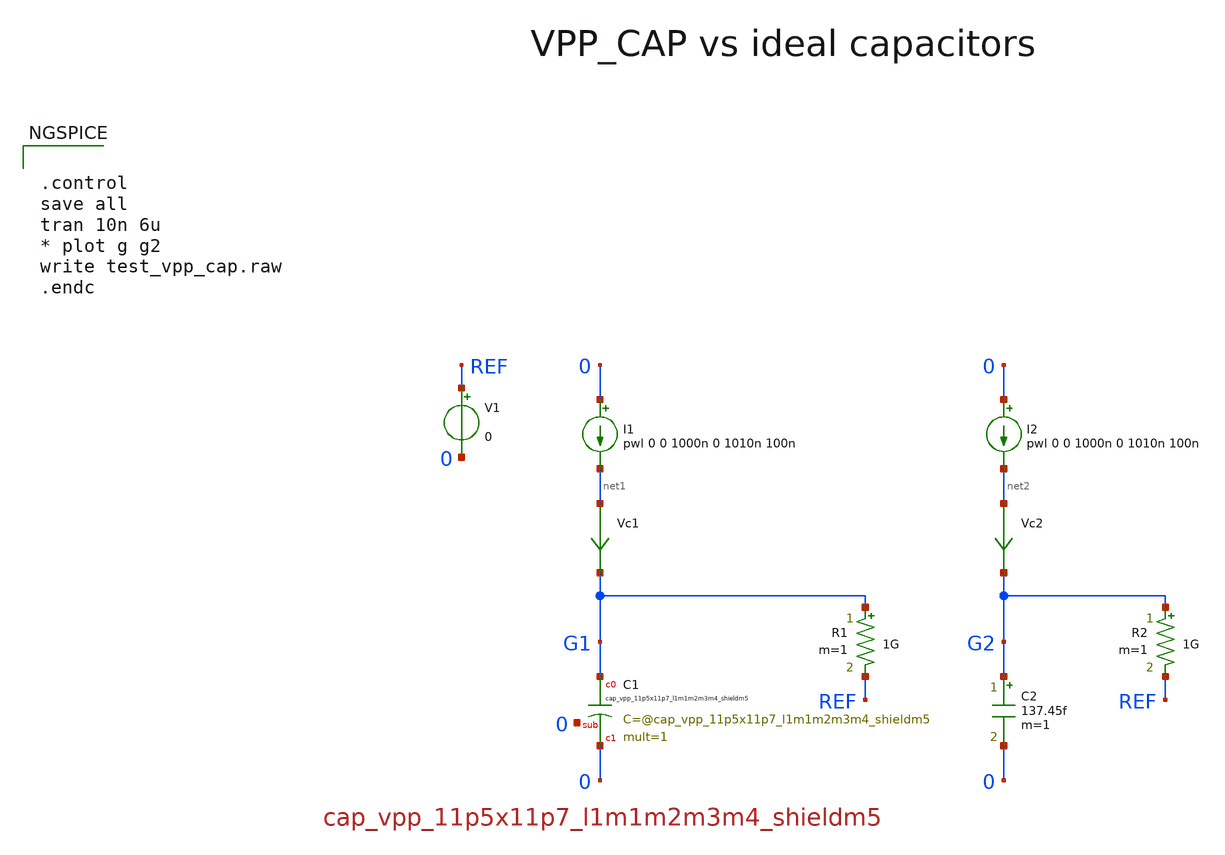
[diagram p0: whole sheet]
** sch_path: testdata/designs/sky130A/cap_vpp_11p5x11p7_l1m1m2m3m4_shieldm5/xschem_vpp_cap_tb.sch
* Copyright 2021 Stefan Frederik Schippers
* Licensed under the Apache License, Version 2.0 (the "License");
* you may not use this file except in compliance with the License.
* You may obtain a copy of the License at
* https://www.apache.org/licenses/LICENSE-2.0
* Unless required by applicable law or agreed to in writing, software
* distributed under the License is distributed on an "AS IS" BASIS,
* WITHOUT WARRANTIES OR CONDITIONS OF ANY KIND, either express or implied.
* See the License for the specific language governing permissions and
* limitations under the License.
**.subckt xschem_vpp_cap_tb
I1 0 net1 pwl 0 0 1000n 0 1010n 100n
R1 G1 REF 1G m=1
C2 G2 0 137.45f m=1
V1 REF 0 0
XC1 G1 0 0 sky130_fd_pr__cap_vpp_11p5x11p7_l1m1m2m3m4_shieldm5 mult=1 m=1
I2 0 net2 pwl 0 0 1000n 0 1010n 100n
R2 G2 REF 1G m=1
Vc1 net1 G1 0
.save i(vc1)
Vc2 net2 G2 0
.save i(vc2)
**** begin user architecture code


.control
save all
tran 10n 6u
* plot g g2
write test_vpp_cap.raw
.endc



** opencircuitdesign pdks install
.lib $::SKYWATER_MODELS/sky130.lib.spice tt


**** end user architecture code
**.ends
.end
